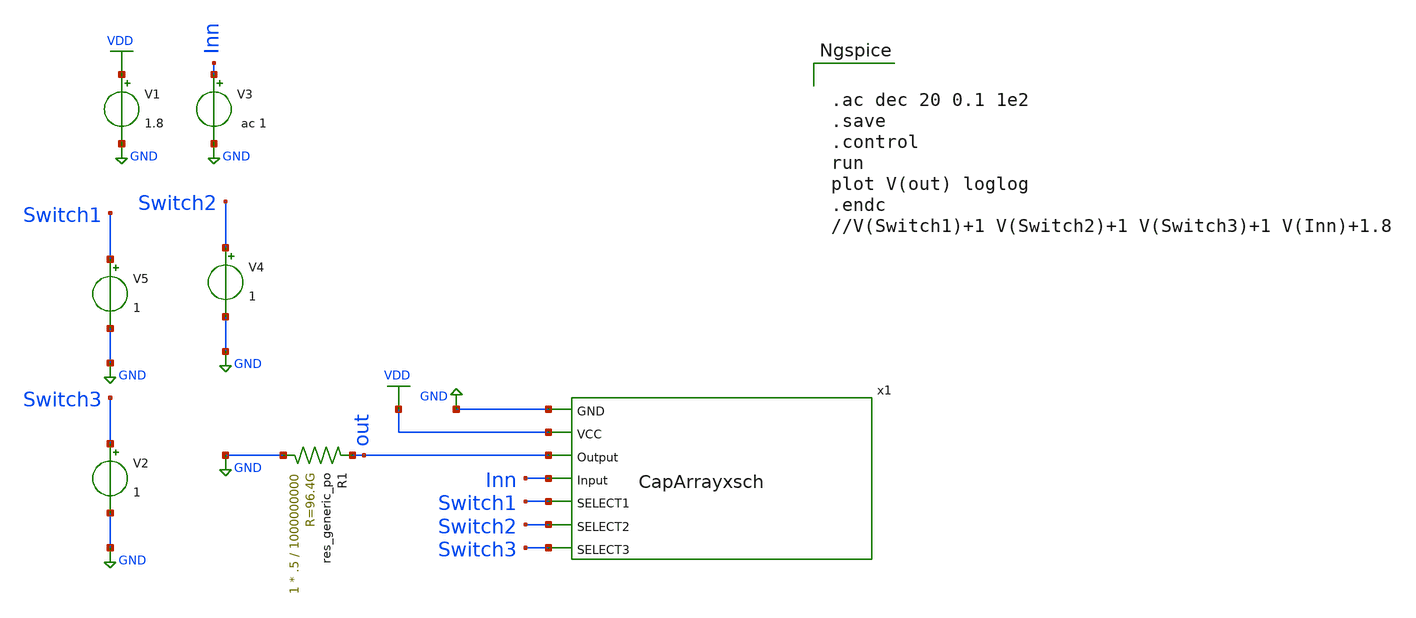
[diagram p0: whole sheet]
** sch_path: sky130_cells/Practice/Capacitor_Array/Schematic/CAPArray_TB.sch
**.subckt CAPArray_TB
x1 GND VDD out Inn Switch1 Switch2 Switch3 CapArrayxsch
V2 Switch3 GND 1
V3 Inn GND ac 1
V1 VDD GND 1.8
V4 Switch2 GND 1
V5 Switch1 GND 1
XR1 GND out sky130_fd_pr__res_generic_po W=.5 L=1000000000 m=1
**** begin user architecture code

** opencircuitdesign pdks install
.lib $::SKYWATER_MODELS/sky130.lib.spice tt




.ac dec 20 0.1 1e2
.save
.control
run
plot V(out) loglog
.endc
//V(Switch1)+1 V(Switch2)+1 V(Switch3)+1 V(Inn)+1.8


**** end user architecture code
**.ends

* expanding   symbol:  sky130_cells/Practice/Capacitor_Array/LVS/CapArrayxsch.sym # of pins=7
** sym_path: sky130_cells/Practice/Capacitor_Array/LVS/CapArrayxsch.sym
** sch_path: sky130_cells/Practice/Capacitor_Array/LVS/CapArrayxsch.sch
.subckt CapArrayxsch GND VCC Output Input SELECT1 SELECT2 SELECT3
*.ipin SELECT1
*.ipin SELECT2
*.ipin SELECT3
*.ipin Output
*.ipin Input
*.ipin GND
*.ipin VCC
x1 VCC net3 SELECT3 Input GND Tgate0.52by0.4
x2 VCC net4 SELECT2 Input GND Tgate0.52by0.4
x3 VCC net1 SELECT1 Input GND Tgate0.52by0.4
x4 VCC Output SELECT1 net6 GND Tgate0.52by0.4
x5 VCC Output SELECT2 net5 GND Tgate0.52by0.4
x6 VCC Output SELECT3 net2 GND Tgate0.52by0.4
XC1[1] net6 net1 sky130_fd_pr__cap_mim_m3_1 W=1.4 L=5 MF=1 m=1
XC1[2] net6 net1 sky130_fd_pr__cap_mim_m3_1 W=1.4 L=5 MF=1 m=1
XC3[1] net1 net6 sky130_fd_pr__cap_mim_m3_2 W=1.4 L=5 MF=1 m=1
XC3[2] net1 net6 sky130_fd_pr__cap_mim_m3_2 W=1.4 L=5 MF=1 m=1
XC2[1] net5 net4 sky130_fd_pr__cap_mim_m3_1 W=1.4 L=5 MF=1 m=1
XC2[2] net5 net4 sky130_fd_pr__cap_mim_m3_1 W=1.4 L=5 MF=1 m=1
XC2[3] net5 net4 sky130_fd_pr__cap_mim_m3_1 W=1.4 L=5 MF=1 m=1
XC2[4] net5 net4 sky130_fd_pr__cap_mim_m3_1 W=1.4 L=5 MF=1 m=1
XC4[1] net4 net5 sky130_fd_pr__cap_mim_m3_2 W=1.4 L=5 MF=1 m=1
XC4[2] net4 net5 sky130_fd_pr__cap_mim_m3_2 W=1.4 L=5 MF=1 m=1
XC4[3] net4 net5 sky130_fd_pr__cap_mim_m3_2 W=1.4 L=5 MF=1 m=1
XC4[4] net4 net5 sky130_fd_pr__cap_mim_m3_2 W=1.4 L=5 MF=1 m=1
XC5[1] net3 net2 sky130_fd_pr__cap_mim_m3_2 W=1.4 L=5 MF=1 m=1
XC5[2] net3 net2 sky130_fd_pr__cap_mim_m3_2 W=1.4 L=5 MF=1 m=1
XC5[3] net3 net2 sky130_fd_pr__cap_mim_m3_2 W=1.4 L=5 MF=1 m=1
XC5[4] net3 net2 sky130_fd_pr__cap_mim_m3_2 W=1.4 L=5 MF=1 m=1
XC5[5] net3 net2 sky130_fd_pr__cap_mim_m3_2 W=1.4 L=5 MF=1 m=1
XC5[6] net3 net2 sky130_fd_pr__cap_mim_m3_2 W=1.4 L=5 MF=1 m=1
XC5[7] net3 net2 sky130_fd_pr__cap_mim_m3_2 W=1.4 L=5 MF=1 m=1
XC5[8] net3 net2 sky130_fd_pr__cap_mim_m3_2 W=1.4 L=5 MF=1 m=1
XC6[1] net2 net3 sky130_fd_pr__cap_mim_m3_1 W=1.4 L=5 MF=1 m=1
XC6[2] net2 net3 sky130_fd_pr__cap_mim_m3_1 W=1.4 L=5 MF=1 m=1
XC6[3] net2 net3 sky130_fd_pr__cap_mim_m3_1 W=1.4 L=5 MF=1 m=1
XC6[4] net2 net3 sky130_fd_pr__cap_mim_m3_1 W=1.4 L=5 MF=1 m=1
XC6[5] net2 net3 sky130_fd_pr__cap_mim_m3_1 W=1.4 L=5 MF=1 m=1
XC6[6] net2 net3 sky130_fd_pr__cap_mim_m3_1 W=1.4 L=5 MF=1 m=1
XC6[7] net2 net3 sky130_fd_pr__cap_mim_m3_1 W=1.4 L=5 MF=1 m=1
XC6[8] net2 net3 sky130_fd_pr__cap_mim_m3_1 W=1.4 L=5 MF=1 m=1
.ends


* expanding   symbol:  sky130_cells/Practice/Capacitor_Array/Schematic/Tgate0.52by0.4.sym # of
*+ pins=5
** sym_path: sky130_cells/Practice/Capacitor_Array/Schematic/Tgate0.52by0.4.sym
** sch_path: sky130_cells/Practice/Capacitor_Array/Schematic/Tgate0.52by0.4.sch
.subckt Tgate0.52by0.4 VPWR OUTPUT SELECT INPUT GND
*.iopin VPWR
*.ipin SELECT
*.iopin INPUT
*.iopin OUTPUT
*.ipin GND
XM5 net1 SELECT GND GND sky130_fd_pr__nfet_g5v0d10v5 L=0.5 W=0.42 nf=1 ad='int((1 + 1)/2) * 0.42 / 1 * 0.29'
+ as='int((1 + 2)/2) * 0.42 / 1 * 0.29' pd='2*int((1 + 1)/2) * (0.42 / 1 + 0.29)' ps='2*int((1 + 2)/2) * (0.42 / 1 + 0.29)'
+ nrd='0.29 / 0.42 ' nrs='0.29 / 0.42 ' sa=0 sb=0 sd=0 mult=1 m=1
XM1 net1 SELECT VPWR VPWR sky130_fd_pr__pfet_g5v0d10v5 L=0.5 W=0.42 nf=1 ad='int((1 + 1)/2) * 0.42 / 1 * 0.29'
+ as='int((1 + 2)/2) * 0.42 / 1 * 0.29' pd='2*int((1 + 1)/2) * (0.42 / 1 + 0.29)' ps='2*int((1 + 2)/2) * (0.42 / 1 + 0.29)'
+ nrd='0.29 / 0.42 ' nrs='0.29 / 0.42 ' sa=0 sb=0 sd=0 mult=1 m=1
XM2 INPUT net1 OUTPUT VPWR sky130_fd_pr__pfet_g5v0d10v5 L=0.5 W=0.42 nf=1 ad='int((1 + 1)/2) * 0.42 / 1 * 0.29'
+ as='int((1 + 2)/2) * 0.42 / 1 * 0.29' pd='2*int((1 + 1)/2) * (0.42 / 1 + 0.29)' ps='2*int((1 + 2)/2) * (0.42 / 1 + 0.29)'
+ nrd='0.29 / 0.42 ' nrs='0.29 / 0.42 ' sa=0 sb=0 sd=0 mult=1 m=1
XM3 OUTPUT SELECT INPUT GND sky130_fd_pr__nfet_g5v0d10v5 L=0.5 W=0.42 nf=1 ad='int((1 + 1)/2) * 0.42 / 1 * 0.29'
+ as='int((1 + 2)/2) * 0.42 / 1 * 0.29' pd='2*int((1 + 1)/2) * (0.42 / 1 + 0.29)' ps='2*int((1 + 2)/2) * (0.42 / 1 + 0.29)'
+ nrd='0.29 / 0.42 ' nrs='0.29 / 0.42 ' sa=0 sb=0 sd=0 mult=1 m=1
.ends

.GLOBAL GND
.GLOBAL VDD
.end
